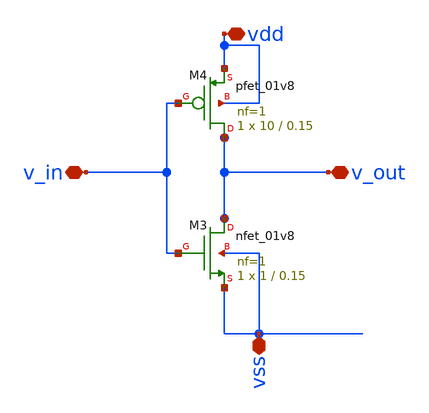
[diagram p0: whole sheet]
** sch_path: Synapse/syn_rep.sch
**.subckt syn_rep v_in vdd vss v_out
*.iopin v_in
*.iopin vdd
*.iopin vss
*.iopin v_out
XM3 v_out v_in vss vss sky130_fd_pr__nfet_01v8 L=0.15 W=1 nf=1 ad='int((nf+1)/2) * W/nf * 0.29' as='int((nf+2)/2) * W/nf * 0.29'
+ pd='2*int((nf+1)/2) * (W/nf + 0.29)' ps='2*int((nf+2)/2) * (W/nf + 0.29)' nrd='0.29 / W' nrs='0.29 / W'
+ sa=0 sb=0 sd=0 mult=1 m=1
XM4 v_out v_in vdd vdd sky130_fd_pr__pfet_01v8 L=0.15 W=10 nf=1 ad='int((nf+1)/2) * W/nf * 0.29' as='int((nf+2)/2) * W/nf * 0.29'
+ pd='2*int((nf+1)/2) * (W/nf + 0.29)' ps='2*int((nf+2)/2) * (W/nf + 0.29)' nrd='0.29 / W' nrs='0.29 / W'
+ sa=0 sb=0 sd=0 mult=1 m=1
**.ends
.end
